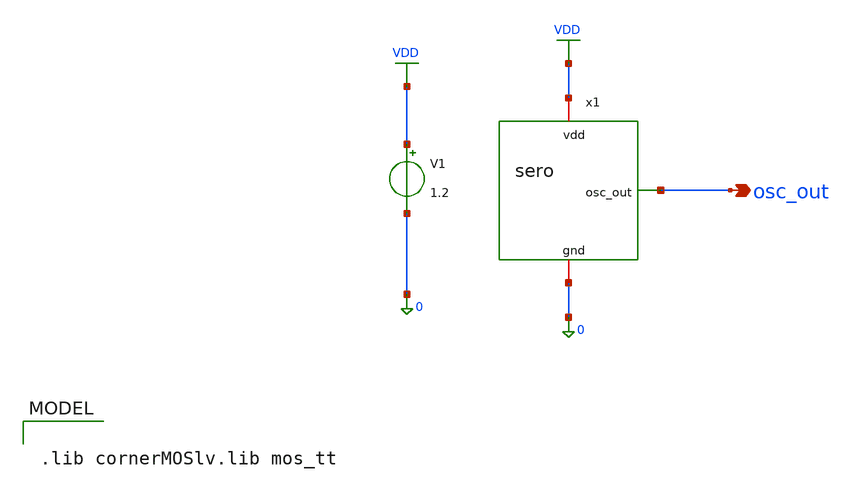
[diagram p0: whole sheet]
** sch_path: simulations/tb/tran_sero.sch
**.subckt tran_sero osc_out
*.opin osc_out
x1 VDD osc_out 0 sero
V1 VDD 0 1.2
**** begin user architecture code

.lib cornerMOSlv.lib mos_tt



.param length=150n
.param temp=27
.control
  save all
  tran 2p 10n

  meas tran t1 when v(osc_out)=0.6 rise=3
  meas tran t2 when v(osc_out)=0.6 rise=4
  let freq = 1 / (t2 - t1)

  echo "========================================================================"
  echo "                SINGLE RUN TRANSIENT PERFORMANCE METRICS                "
  echo "========================================================================"
  print freq
  echo "========================================================================"

  write tran_sero.raw
.endc


**** end user architecture code
**.ends
.GLOBAL VDD
.end
